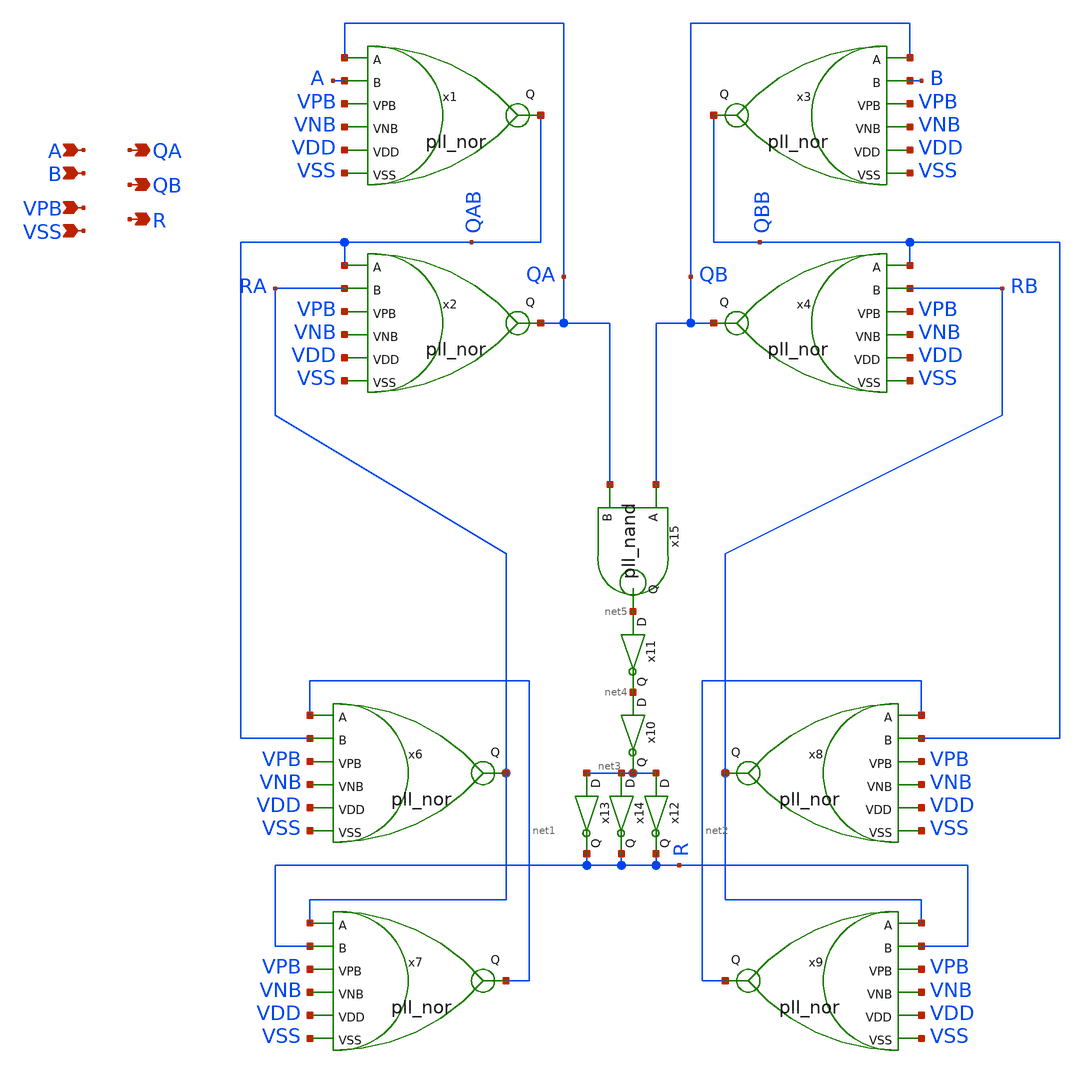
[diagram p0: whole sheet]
** sch_path: xschem/pll_pfd.sch
**.subckt pll_pfd A B VPB VSS QA QB R
*.ipin A
*.ipin B
*.ipin VPB
*.ipin VSS
*.opin QA
*.opin QB
*.opin R
x1 QA A VPB VNB VDD QAB VSS pll_nor
x2 QAB RA VPB VNB VDD QA VSS pll_nor
x3 QB B VPB VNB VDD QBB VSS pll_nor
x4 QBB RB VPB VNB VDD QB VSS pll_nor
x6 net1 QAB VPB VNB VDD RA VSS pll_nor
x7 RA R VPB VNB VDD net1 VSS pll_nor
x8 net2 QBB VPB VNB VDD RB VSS pll_nor
x9 RB R VPB VNB VDD net2 VSS pll_nor
x10 net4 net3 VDD VSS pll_inv1
x11 net5 net4 VDD VSS pll_inv1
x12 net3 R VDD VSS pll_inv1
x13 net3 R VDD VSS pll_inv1
x14 net3 R VDD VSS pll_inv1
x15 QB QA net5 VSS VDD pll_nand
**.ends
.end
